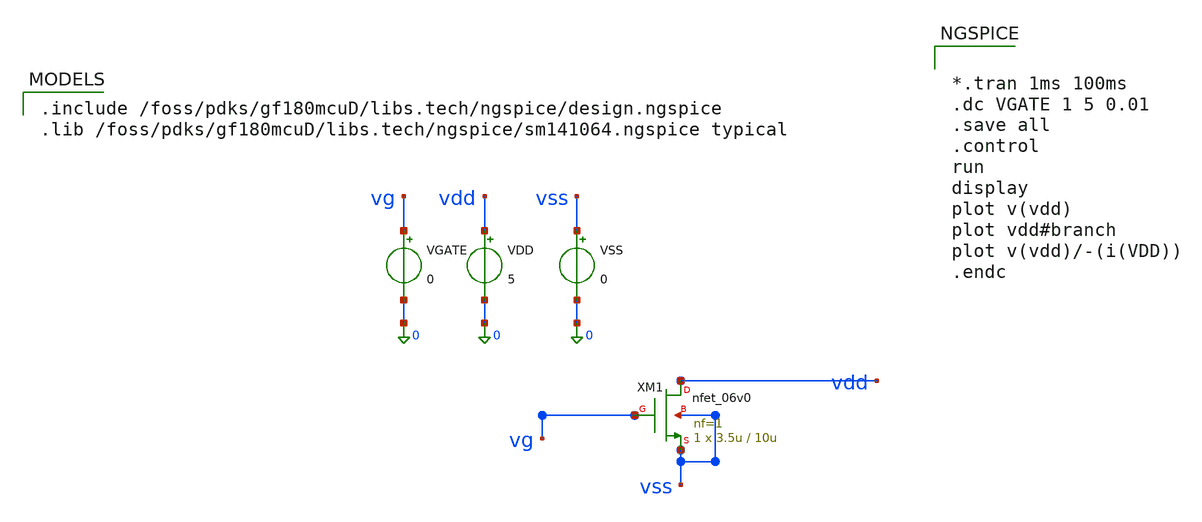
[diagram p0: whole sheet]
** sch_path: activities/opamp3An/490k_NMOSresistor_tb.sch
**.subckt 490k_NMOSresistor_tb
VGATE vg 0 0
VDD vdd 0 5
VSS vss 0 0
XM1 vdd vg vss vss nfet_06v0 L=10u W=3.5u nf=1 ad='int((nf+1)/2) * W/nf * 0.18u' as='int((nf+2)/2) * W/nf * 0.18u'
+ pd='2*int((nf+1)/2) * (W/nf + 0.18u)' ps='2*int((nf+2)/2) * (W/nf + 0.18u)' nrd='0.18u / W' nrs='0.18u / W'
+ sa=0 sb=0 sd=0 m=1
**** begin user architecture code

.include /foss/pdks/gf180mcuD/libs.tech/ngspice/design.ngspice
.lib /foss/pdks/gf180mcuD/libs.tech/ngspice/sm141064.ngspice typical



*.tran 1ms 100ms
.dc VGATE 1 5 0.01
.save all
.control
run
display
plot v(vdd)
plot vdd#branch
plot v(vdd)/-(i(VDD))
.endc


**** end user architecture code
**.ends
.end
